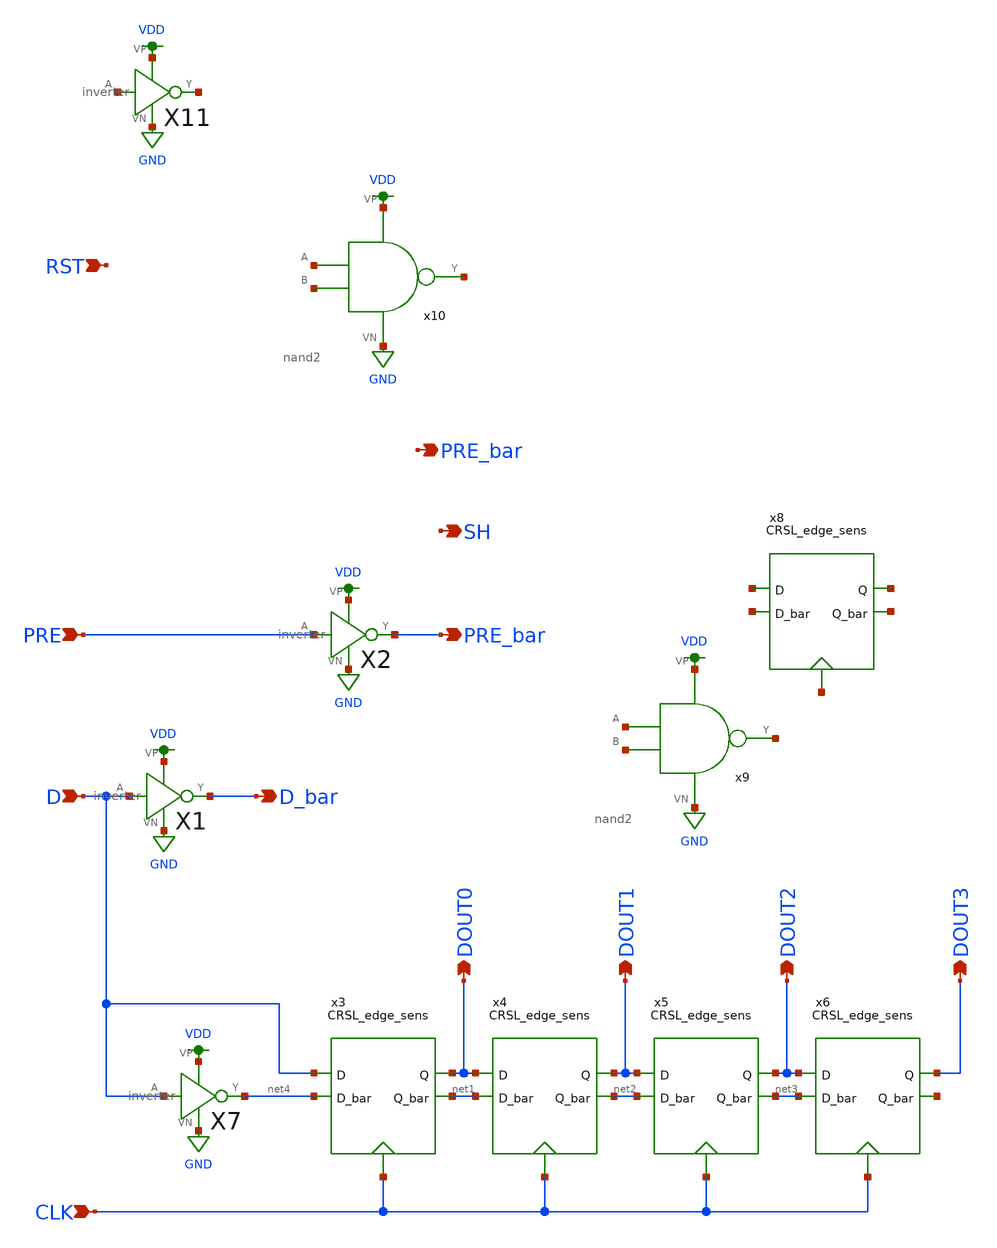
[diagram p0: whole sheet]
** sch_path: schematics/digital_control.sch
**.subckt digital_control D D_bar PRE_bar SH DOUT0 DOUT1 DOUT2 DOUT3 CLK PRE PRE_bar RST
*.ipin D
*.opin D_bar
*.opin PRE_bar
*.opin SH
*.opin DOUT0
*.opin DOUT1
*.opin DOUT2
*.opin DOUT3
*.ipin CLK
*.ipin PRE
*.opin PRE_bar
*.ipin RST
X1 D D_bar VDD GND inverter
X2 PRE PRE_bar VDD GND inverter
x3 CLK DOUT0 D net1 net4 CRSL_edge_sens
x4 CLK DOUT1 DOUT0 net2 net1 CRSL_edge_sens
x5 CLK DOUT2 DOUT1 net3 net2 CRSL_edge_sens
x6 CLK DOUT3 DOUT2 net5 net3 CRSL_edge_sens
X7 D net4 VDD GND inverter
x8 net6 net7 net8 net9 net10 CRSL_edge_sens
x9 VDD net11 net12 net13 GND nand2
x10 VDD net14 net15 net16 GND nand2
X11 net17 net18 VDD GND inverter
**.ends

* expanding   symbol:  ./inverter.sym # of pins=4
** sym_path: schematics/inverter.sym
** sch_path: schematics/inverter.sch
.subckt inverter A Y VP VN
*.ipin A
*.iopin VP
*.iopin VN
*.opin Y
XM1 Y A VP VDD sky130_fd_pr__pfet_01v8 L=0.15 W=1 nf=1 ad='int((nf+1)/2) * W/nf * 0.29' as='int((nf+2)/2) * W/nf * 0.29'
+ pd='2*int((nf+1)/2) * (W/nf + 0.29)' ps='2*int((nf+2)/2) * (W/nf + 0.29)' nrd='0.29 / W' nrs='0.29 / W'
+ sa=0 sb=0 sd=0 mult=1 m=1
XM2 Y A VN GND sky130_fd_pr__nfet_01v8 L=0.15 W=1 nf=1 ad='int((nf+1)/2) * W/nf * 0.29' as='int((nf+2)/2) * W/nf * 0.29'
+ pd='2*int((nf+1)/2) * (W/nf + 0.29)' ps='2*int((nf+2)/2) * (W/nf + 0.29)' nrd='0.29 / W' nrs='0.29 / W'
+ sa=0 sb=0 sd=0 mult=1 m=1
.ends


* expanding   symbol:
*+  /home/madvlsi/Documents/algorithmic-ada-converter/schematics/CRSL_edge_sens.sym # of pins=5
** sym_path: schematics/CRSL_edge_sens.sym
** sch_path: schematics/CRSL_edge_sens.sch
.subckt CRSL_edge_sens Phi Q D Q_bar D_bar
*.ipin D
*.ipin D_bar
*.opin Q
*.opin Q_bar
*.ipin Phi
XM14 Q_bar Q GND GND sky130_fd_pr__nfet_01v8 L=0.15 W=1 nf=1 ad='int((nf+1)/2) * W/nf * 0.29' as='int((nf+2)/2) * W/nf * 0.29'
+ pd='2*int((nf+1)/2) * (W/nf + 0.29)' ps='2*int((nf+2)/2) * (W/nf + 0.29)' nrd='0.29 / W' nrs='0.29 / W'
+ sa=0 sb=0 sd=0 mult=1 m=1
XM2 Q_bar Phi net3 GND sky130_fd_pr__nfet_01v8 L=0.15 W=1 nf=1 ad='int((nf+1)/2) * W/nf * 0.29' as='int((nf+2)/2) * W/nf * 0.29'
+ pd='2*int((nf+1)/2) * (W/nf + 0.29)' ps='2*int((nf+2)/2) * (W/nf + 0.29)' nrd='0.29 / W' nrs='0.29 / W'
+ sa=0 sb=0 sd=0 mult=1 m=1
XM6 Q Phi net2 GND sky130_fd_pr__nfet_01v8 L=0.15 W=1 nf=1 ad='int((nf+1)/2) * W/nf * 0.29' as='int((nf+2)/2) * W/nf * 0.29'
+ pd='2*int((nf+1)/2) * (W/nf + 0.29)' ps='2*int((nf+2)/2) * (W/nf + 0.29)' nrd='0.29 / W' nrs='0.29 / W'
+ sa=0 sb=0 sd=0 mult=1 m=1
XM7 net4 Phi GND GND sky130_fd_pr__nfet_01v8 L=0.15 W=4 nf=1 ad='int((nf+1)/2) * W/nf * 0.29' as='int((nf+2)/2) * W/nf * 0.29'
+ pd='2*int((nf+1)/2) * (W/nf + 0.29)' ps='2*int((nf+2)/2) * (W/nf + 0.29)' nrd='0.29 / W' nrs='0.29 / W'
+ sa=0 sb=0 sd=0 mult=1 m=1
XM8 net3 net2 net4 GND sky130_fd_pr__nfet_01v8 L=0.15 W=1 nf=1 ad='int((nf+1)/2) * W/nf * 0.29' as='int((nf+2)/2) * W/nf * 0.29'
+ pd='2*int((nf+1)/2) * (W/nf + 0.29)' ps='2*int((nf+2)/2) * (W/nf + 0.29)' nrd='0.29 / W' nrs='0.29 / W'
+ sa=0 sb=0 sd=0 mult=1 m=1
XM12 net3 net2 VDD VDD sky130_fd_pr__pfet_01v8 L=0.15 W=1 nf=1 ad='int((nf+1)/2) * W/nf * 0.29' as='int((nf+2)/2) * W/nf * 0.29'
+ pd='2*int((nf+1)/2) * (W/nf + 0.29)' ps='2*int((nf+2)/2) * (W/nf + 0.29)' nrd='0.29 / W' nrs='0.29 / W'
+ sa=0 sb=0 sd=0 mult=1 m=1
XM9 net2 net3 VDD VDD sky130_fd_pr__pfet_01v8 L=0.15 W=1 nf=1 ad='int((nf+1)/2) * W/nf * 0.29' as='int((nf+2)/2) * W/nf * 0.29'
+ pd='2*int((nf+1)/2) * (W/nf + 0.29)' ps='2*int((nf+2)/2) * (W/nf + 0.29)' nrd='0.29 / W' nrs='0.29 / W'
+ sa=0 sb=0 sd=0 mult=1 m=1
XM1 net1 Phi VDD VDD sky130_fd_pr__pfet_01v8 L=0.15 W=4 nf=1 ad='int((nf+1)/2) * W/nf * 0.29' as='int((nf+2)/2) * W/nf * 0.29'
+ pd='2*int((nf+1)/2) * (W/nf + 0.29)' ps='2*int((nf+2)/2) * (W/nf + 0.29)' nrd='0.29 / W' nrs='0.29 / W'
+ sa=0 sb=0 sd=0 mult=1 m=1
XM3 Q_bar Q net1 VDD sky130_fd_pr__pfet_01v8 L=0.15 W=1 nf=1 ad='int((nf+1)/2) * W/nf * 0.29' as='int((nf+2)/2) * W/nf * 0.29'
+ pd='2*int((nf+1)/2) * (W/nf + 0.29)' ps='2*int((nf+2)/2) * (W/nf + 0.29)' nrd='0.29 / W' nrs='0.29 / W'
+ sa=0 sb=0 sd=0 mult=1 m=1
XM4 Q Q_bar net1 VDD sky130_fd_pr__pfet_01v8 L=0.15 W=1 nf=1 ad='int((nf+1)/2) * W/nf * 0.29' as='int((nf+2)/2) * W/nf * 0.29'
+ pd='2*int((nf+1)/2) * (W/nf + 0.29)' ps='2*int((nf+2)/2) * (W/nf + 0.29)' nrd='0.29 / W' nrs='0.29 / W'
+ sa=0 sb=0 sd=0 mult=1 m=1
XM10 Q Q_bar GND GND sky130_fd_pr__nfet_01v8 L=0.15 W=1 nf=1 ad='int((nf+1)/2) * W/nf * 0.29' as='int((nf+2)/2) * W/nf * 0.29'
+ pd='2*int((nf+1)/2) * (W/nf + 0.29)' ps='2*int((nf+2)/2) * (W/nf + 0.29)' nrd='0.29 / W' nrs='0.29 / W'
+ sa=0 sb=0 sd=0 mult=1 m=1
XM5 net2 net3 net4 GND sky130_fd_pr__nfet_01v8 L=0.15 W=1 nf=1 ad='int((nf+1)/2) * W/nf * 0.29' as='int((nf+2)/2) * W/nf * 0.29'
+ pd='2*int((nf+1)/2) * (W/nf + 0.29)' ps='2*int((nf+2)/2) * (W/nf + 0.29)' nrd='0.29 / W' nrs='0.29 / W'
+ sa=0 sb=0 sd=0 mult=1 m=1
XM11 net3 Phi D_bar VDD sky130_fd_pr__pfet_01v8 L=0.15 W=1 nf=1 ad='int((nf+1)/2) * W/nf * 0.29' as='int((nf+2)/2) * W/nf * 0.29'
+ pd='2*int((nf+1)/2) * (W/nf + 0.29)' ps='2*int((nf+2)/2) * (W/nf + 0.29)' nrd='0.29 / W' nrs='0.29 / W'
+ sa=0 sb=0 sd=0 mult=1 m=1
XM15 net2 Phi D VDD sky130_fd_pr__pfet_01v8 L=0.15 W=1 nf=1 ad='int((nf+1)/2) * W/nf * 0.29' as='int((nf+2)/2) * W/nf * 0.29'
+ pd='2*int((nf+1)/2) * (W/nf + 0.29)' ps='2*int((nf+2)/2) * (W/nf + 0.29)' nrd='0.29 / W' nrs='0.29 / W'
+ sa=0 sb=0 sd=0 mult=1 m=1
.ends


* expanding   symbol:  /home/madvlsi/Documents/algorithmic-ada-converter/schematics/nand2.sym # of
*+ pins=5
** sym_path: schematics/nand2.sym
** sch_path: schematics/nand2.sch
.subckt nand2 VP B Y A VN
*.iopin VP
*.iopin VN
*.ipin A
*.ipin B
*.opin Y
XM5 Y B VP VP sky130_fd_pr__pfet_01v8 L=0.15 W=1 nf=1 ad='int((nf+1)/2) * W/nf * 0.29' as='int((nf+2)/2) * W/nf * 0.29'
+ pd='2*int((nf+1)/2) * (W/nf + 0.29)' ps='2*int((nf+2)/2) * (W/nf + 0.29)' nrd='0.29 / W' nrs='0.29 / W'
+ sa=0 sb=0 sd=0 mult=1 m=1
XM2 Y A VP VP sky130_fd_pr__pfet_01v8 L=0.15 W=1 nf=1 ad='int((nf+1)/2) * W/nf * 0.29' as='int((nf+2)/2) * W/nf * 0.29'
+ pd='2*int((nf+1)/2) * (W/nf + 0.29)' ps='2*int((nf+2)/2) * (W/nf + 0.29)' nrd='0.29 / W' nrs='0.29 / W'
+ sa=0 sb=0 sd=0 mult=1 m=1
XM1 Y A net1 VN sky130_fd_pr__nfet_01v8 L=0.15 W=1 nf=1 ad='int((nf+1)/2) * W/nf * 0.29' as='int((nf+2)/2) * W/nf * 0.29'
+ pd='2*int((nf+1)/2) * (W/nf + 0.29)' ps='2*int((nf+2)/2) * (W/nf + 0.29)' nrd='0.29 / W' nrs='0.29 / W'
+ sa=0 sb=0 sd=0 mult=1 m=1
XM3 net1 B VN VN sky130_fd_pr__nfet_01v8 L=0.15 W=1 nf=1 ad='int((nf+1)/2) * W/nf * 0.29' as='int((nf+2)/2) * W/nf * 0.29'
+ pd='2*int((nf+1)/2) * (W/nf + 0.29)' ps='2*int((nf+2)/2) * (W/nf + 0.29)' nrd='0.29 / W' nrs='0.29 / W'
+ sa=0 sb=0 sd=0 mult=1 m=1
.ends

.GLOBAL VDD
.GLOBAL GND
.end
